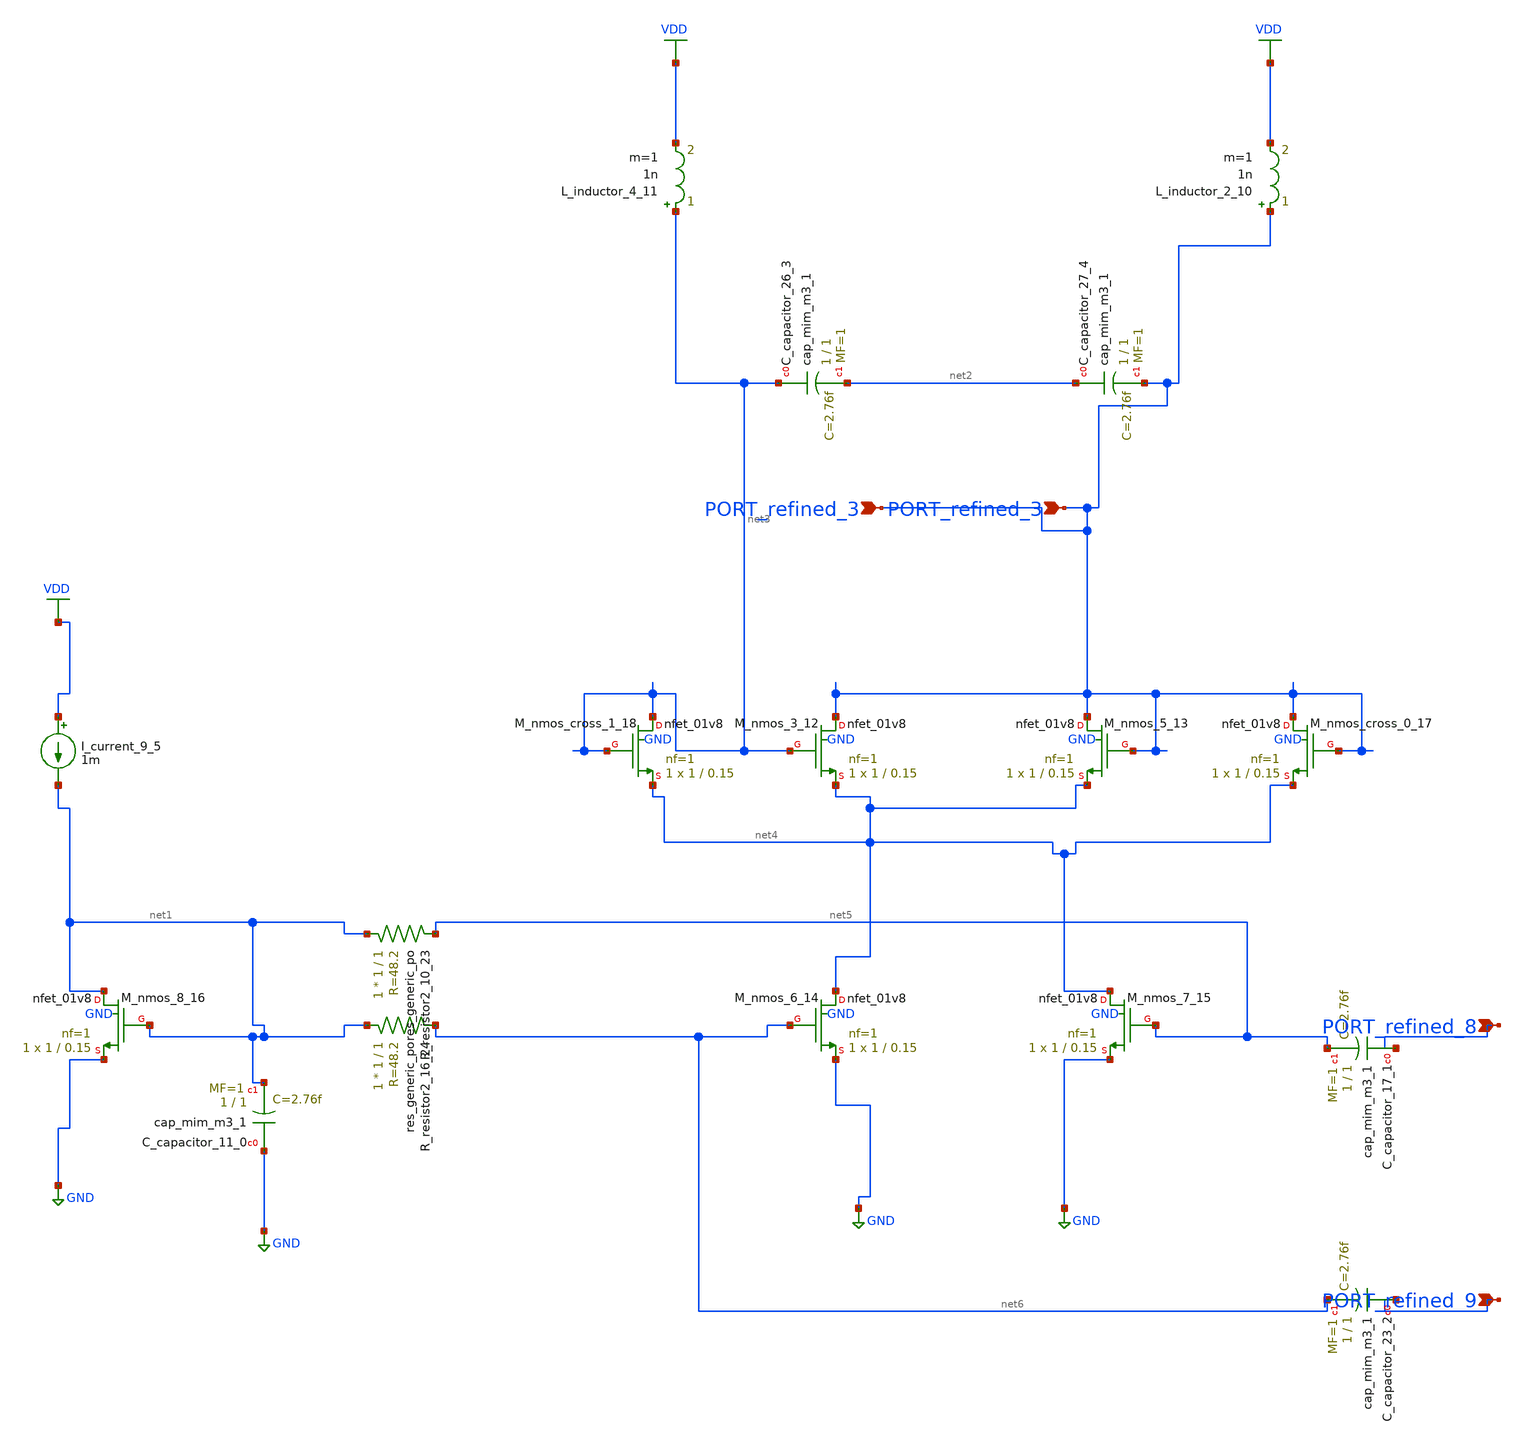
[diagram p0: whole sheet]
** sch_path: schematics/SchemGen/10_1007_s10470-024-02258-z_04_002.sch
**.subckt 10_1007_s10470-024-02258-z_04_002 PORT_refined_3 PORT_refined_9 PORT_refined_8
*+ PORT_refined_3
*.ipin PORT_refined_3
*.ipin PORT_refined_9
*.ipin PORT_refined_8
*.ipin PORT_refined_3
XC_capacitor_11_0 GND net1 sky130_fd_pr__cap_mim_m3_1 W=1 L=1 MF=1 m=1
XC_capacitor_17_1 PORT_refined_8 net5 sky130_fd_pr__cap_mim_m3_1 W=1 L=1 MF=1 m=1
XC_capacitor_23_2 PORT_refined_9 net6 sky130_fd_pr__cap_mim_m3_1 W=1 L=1 MF=1 m=1
XC_capacitor_26_3 net3 net2 sky130_fd_pr__cap_mim_m3_1 W=1 L=1 MF=1 m=1
XC_capacitor_27_4 net2 PORT_refined_3 sky130_fd_pr__cap_mim_m3_1 W=1 L=1 MF=1 m=1
I_current_9_5 VDD net1 1m
L_inductor_2_10 PORT_refined_3 VDD 1n m=1
L_inductor_4_11 net3 VDD 1n m=1
XM_nmos_3_12 PORT_refined_3 net3 net4 GND sky130_fd_pr__nfet_01v8 L=0.15 W=1 nf=1 ad='int((1 + 1)/2) * 1 / 1 * 0.29'
+ as='int((1 + 2)/2) * 1 / 1 * 0.29' pd='2*int((1 + 1)/2) * (1 / 1 + 0.29)' ps='2*int((1 + 2)/2) * (1 / 1 + 0.29)'
+ nrd='0.29 / 1 ' nrs='0.29 / 1 ' sa=0 sb=0 sd=0 mult=1 m=1
XM_nmos_5_13 PORT_refined_3 PORT_refined_3 net4 GND sky130_fd_pr__nfet_01v8 L=0.15 W=1 nf=1 ad='int((1 + 1)/2) * 1 / 1 * 0.29'
+ as='int((1 + 2)/2) * 1 / 1 * 0.29' pd='2*int((1 + 1)/2) * (1 / 1 + 0.29)' ps='2*int((1 + 2)/2) * (1 / 1 + 0.29)'
+ nrd='0.29 / 1 ' nrs='0.29 / 1 ' sa=0 sb=0 sd=0 mult=1 m=1
XM_nmos_6_14 net4 net6 GND GND sky130_fd_pr__nfet_01v8 L=0.15 W=1 nf=1 ad='int((1 + 1)/2) * 1 / 1 * 0.29'
+ as='int((1 + 2)/2) * 1 / 1 * 0.29' pd='2*int((1 + 1)/2) * (1 / 1 + 0.29)' ps='2*int((1 + 2)/2) * (1 / 1 + 0.29)'
+ nrd='0.29 / 1 ' nrs='0.29 / 1 ' sa=0 sb=0 sd=0 mult=1 m=1
XM_nmos_7_15 net4 net5 GND GND sky130_fd_pr__nfet_01v8 L=0.15 W=1 nf=1 ad='int((1 + 1)/2) * 1 / 1 * 0.29'
+ as='int((1 + 2)/2) * 1 / 1 * 0.29' pd='2*int((1 + 1)/2) * (1 / 1 + 0.29)' ps='2*int((1 + 2)/2) * (1 / 1 + 0.29)'
+ nrd='0.29 / 1 ' nrs='0.29 / 1 ' sa=0 sb=0 sd=0 mult=1 m=1
XM_nmos_8_16 net1 net1 GND GND sky130_fd_pr__nfet_01v8 L=0.15 W=1 nf=1 ad='int((1 + 1)/2) * 1 / 1 * 0.29'
+ as='int((1 + 2)/2) * 1 / 1 * 0.29' pd='2*int((1 + 1)/2) * (1 / 1 + 0.29)' ps='2*int((1 + 2)/2) * (1 / 1 + 0.29)'
+ nrd='0.29 / 1 ' nrs='0.29 / 1 ' sa=0 sb=0 sd=0 mult=1 m=1
XM_nmos_cross_0_17 PORT_refined_3 PORT_refined_3 net4 GND sky130_fd_pr__nfet_01v8 L=0.15 W=1 nf=1 ad='int((1 + 1)/2) * 1 / 1 * 0.29'
+ as='int((1 + 2)/2) * 1 / 1 * 0.29' pd='2*int((1 + 1)/2) * (1 / 1 + 0.29)' ps='2*int((1 + 2)/2) * (1 / 1 + 0.29)'
+ nrd='0.29 / 1 ' nrs='0.29 / 1 ' sa=0 sb=0 sd=0 mult=1 m=1
XM_nmos_cross_1_18 net3 net3 net4 GND sky130_fd_pr__nfet_01v8 L=0.15 W=1 nf=1 ad='int((1 + 1)/2) * 1 / 1 * 0.29'
+ as='int((1 + 2)/2) * 1 / 1 * 0.29' pd='2*int((1 + 1)/2) * (1 / 1 + 0.29)' ps='2*int((1 + 2)/2) * (1 / 1 + 0.29)'
+ nrd='0.29 / 1 ' nrs='0.29 / 1 ' sa=0 sb=0 sd=0 mult=1 m=1
XR_resistor2_10_23 net1 net5 sky130_fd_pr__res_generic_po W=1 L=1 m=1
XR_resistor2_16_24 net1 net6 sky130_fd_pr__res_generic_po W=1 L=1 m=1
**.ends
.GLOBAL GND
.GLOBAL VDD
.end
